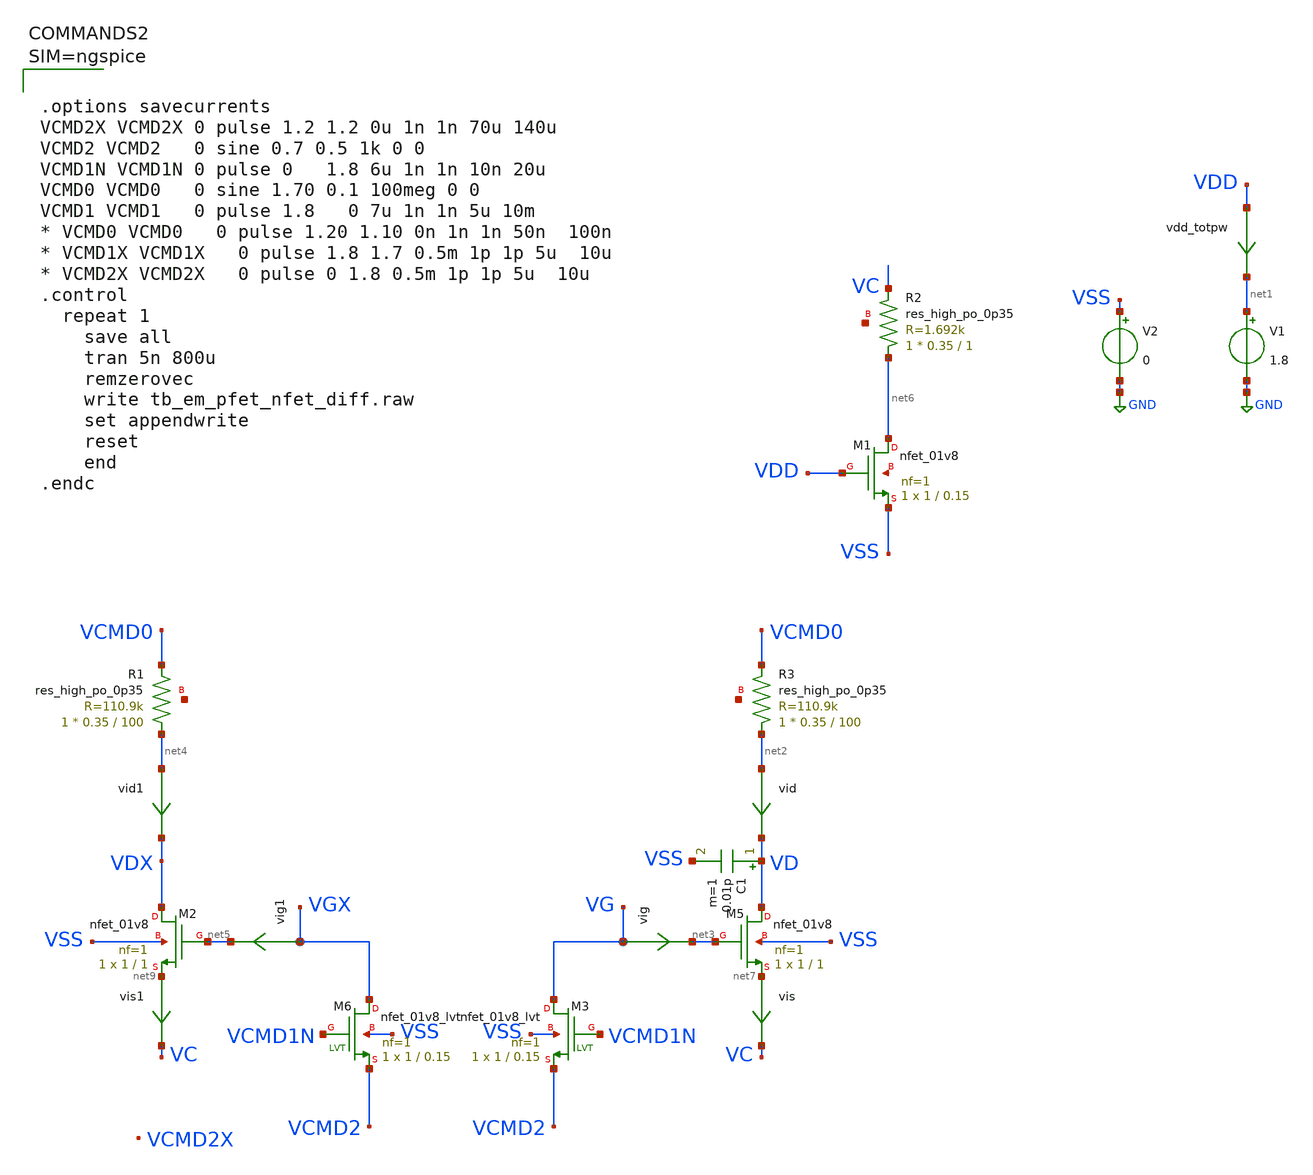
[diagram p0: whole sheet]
** sch_path: xschem/tb_em_pfet_nfet_diff.sch
**.subckt tb_em_pfet_nfet_diff
V1 net1 GND 1.8
V2 VSS GND 0
vdd_totpw VDD net1 0
.save i(vdd_totpw)
vis net7 VC 0
.save i(vis)
XR3 net2 VCMD0 net8 sky130_fd_pr__res_high_po_0p35 L=100 mult=1 m=1
vig VG net3 0
.save i(vig)
vid net2 VD 0
.save i(vid)
vis1 net9 VC 0
.save i(vis1)
XR1 net4 VCMD0 net10 sky130_fd_pr__res_high_po_0p35 L=100 mult=1 m=1
vig1 VGX net5 0
.save i(vig1)
vid1 net4 VDX 0
.save i(vid1)
XM1 net6 VDD VSS net11 sky130_fd_pr__nfet_01v8 L=0.15 W=1 nf=1 ad='int((nf+1)/2) * W/nf * 0.29' as='int((nf+2)/2) * W/nf * 0.29'
+ pd='2*int((nf+1)/2) * (W/nf + 0.29)' ps='2*int((nf+2)/2) * (W/nf + 0.29)' nrd='0.29 / W' nrs='0.29 / W'
+ sa=0 sb=0 sd=0 mult=1 m=1
XR2 net6 VC net12 sky130_fd_pr__res_high_po_0p35 L=1 mult=1 m=1
XM5 VD net3 net7 VSS sky130_fd_pr__nfet_01v8 L=1 W=1 nf=1 ad='int((nf+1)/2) * W/nf * 0.29' as='int((nf+2)/2) * W/nf * 0.29'
+ pd='2*int((nf+1)/2) * (W/nf + 0.29)' ps='2*int((nf+2)/2) * (W/nf + 0.29)' nrd='0.29 / W' nrs='0.29 / W'
+ sa=0 sb=0 sd=0 mult=1 m=1
XM6 VGX VCMD1N VCMD2 VSS sky130_fd_pr__nfet_01v8_lvt L=0.15 W=1 nf=1 ad='int((nf+1)/2) * W/nf * 0.29'
+ as='int((nf+2)/2) * W/nf * 0.29' pd='2*int((nf+1)/2) * (W/nf + 0.29)' ps='2*int((nf+2)/2) * (W/nf + 0.29)'
+ nrd='0.29 / W' nrs='0.29 / W' sa=0 sb=0 sd=0 mult=1 m=1
XM2 VDX net5 net9 VSS sky130_fd_pr__nfet_01v8 L=1 W=1 nf=1 ad='int((nf+1)/2) * W/nf * 0.29' as='int((nf+2)/2) * W/nf * 0.29'
+ pd='2*int((nf+1)/2) * (W/nf + 0.29)' ps='2*int((nf+2)/2) * (W/nf + 0.29)' nrd='0.29 / W' nrs='0.29 / W'
+ sa=0 sb=0 sd=0 mult=1 m=1
XM3 VG VCMD1N VCMD2 VSS sky130_fd_pr__nfet_01v8_lvt L=0.15 W=1 nf=1 ad='int((nf+1)/2) * W/nf * 0.29'
+ as='int((nf+2)/2) * W/nf * 0.29' pd='2*int((nf+1)/2) * (W/nf + 0.29)' ps='2*int((nf+2)/2) * (W/nf + 0.29)'
+ nrd='0.29 / W' nrs='0.29 / W' sa=0 sb=0 sd=0 mult=1 m=1
C1 VD VSS 0.01p m=1
**** begin user architecture code

** opencircuitdesign pdks install
.lib $::SKYWATER_MODELS/sky130.lib.spice tt_mm
*.lib $::SKYWATER_STDCELLS/sky130_fd_sc_hd_blablabla.spice

.subckt sky130_fd_sc_hd__inv_1 A VGND VNB VPB VPWR Y
X0 VGND A Y VNB sky130_fd_pr__nfet_01v8 w=650000u l=150000u
X1 VPWR A Y VPB sky130_fd_pr__pfet_01v8_hvt w=1e+06u l=150000u
.ends





.options savecurrents
VCMD2X VCMD2X 0 pulse 1.2 1.2 0u 1n 1n 70u 140u
VCMD2 VCMD2   0 sine 0.7 0.5 1k 0 0
VCMD1N VCMD1N 0 pulse 0   1.8 6u 1n 1n 10n 20u
VCMD0 VCMD0   0 sine 1.70 0.1 100meg 0 0
VCMD1 VCMD1   0 pulse 1.8   0 7u 1n 1n 5u 10m
* VCMD0 VCMD0   0 pulse 1.20 1.10 0n 1n 1n 50n  100n
* VCMD1X VCMD1X   0 pulse 1.8 1.7 0.5m 1p 1p 5u  10u
* VCMD2X VCMD2X   0 pulse 0 1.8 0.5m 1p 1p 5u  10u
.control
  repeat 1
    save all
    tran 5n 800u
    remzerovec
    write tb_em_pfet_nfet_diff.raw
    set appendwrite
    reset
    end
.endc



**** end user architecture code
**.ends
.GLOBAL GND
.end
